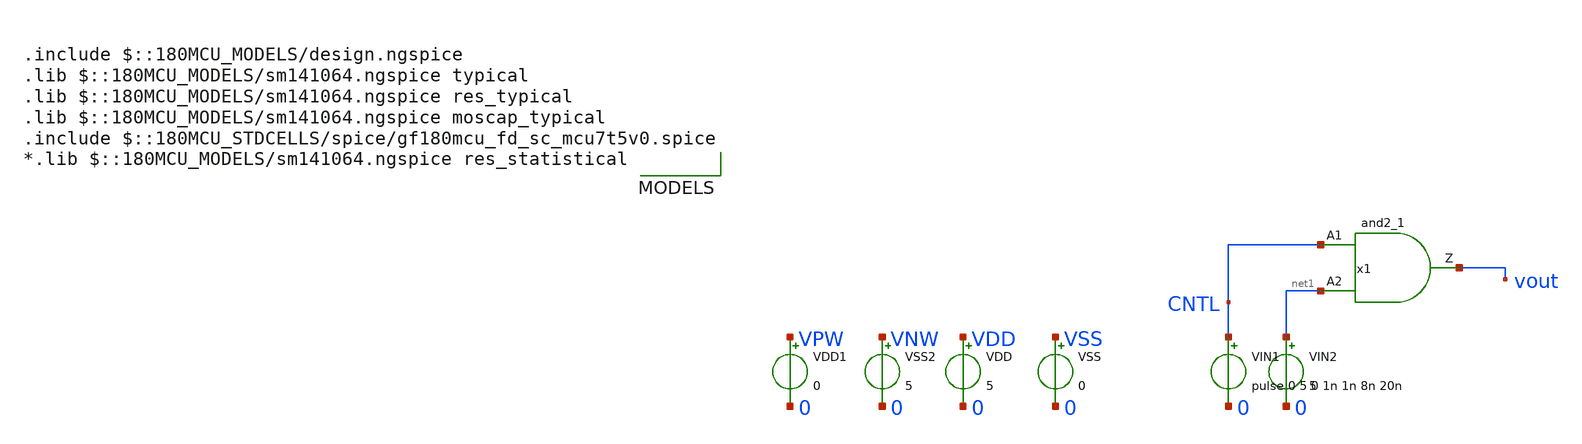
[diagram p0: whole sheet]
** sch_path: xschem/std_cell/Test_and2.sch
**.subckt Test_and2
VIN1 CNTL 0 pulse 0 5 0 1n 1n 8n 20n
VIN2 net1 0 5
VDD VDD 0 5
VSS VSS 0 0
VDD1 VPW 0 0
VSS2 VNW 0 5
x1 CNTL net1 vout VDD VNW VPW VSS gf180mcu_fd_sc_mcu7t5v0__and2_1
**** begin user architecture code




.control
	tran 0.1n 50n
	*dc vin1 0 3.3 0.1
	plot v(CNTL) V(vout)
	plot v(vout)
	write test_and.raw

.endc
.save all





.include $::180MCU_MODELS/design.ngspice
.lib $::180MCU_MODELS/sm141064.ngspice typical
.lib $::180MCU_MODELS/sm141064.ngspice res_typical
.lib $::180MCU_MODELS/sm141064.ngspice moscap_typical
.include $::180MCU_STDCELLS/spice/gf180mcu_fd_sc_mcu7t5v0.spice
*.lib $::180MCU_MODELS/sm141064.ngspice res_statistical

**** end user architecture code
**.ends
.end
